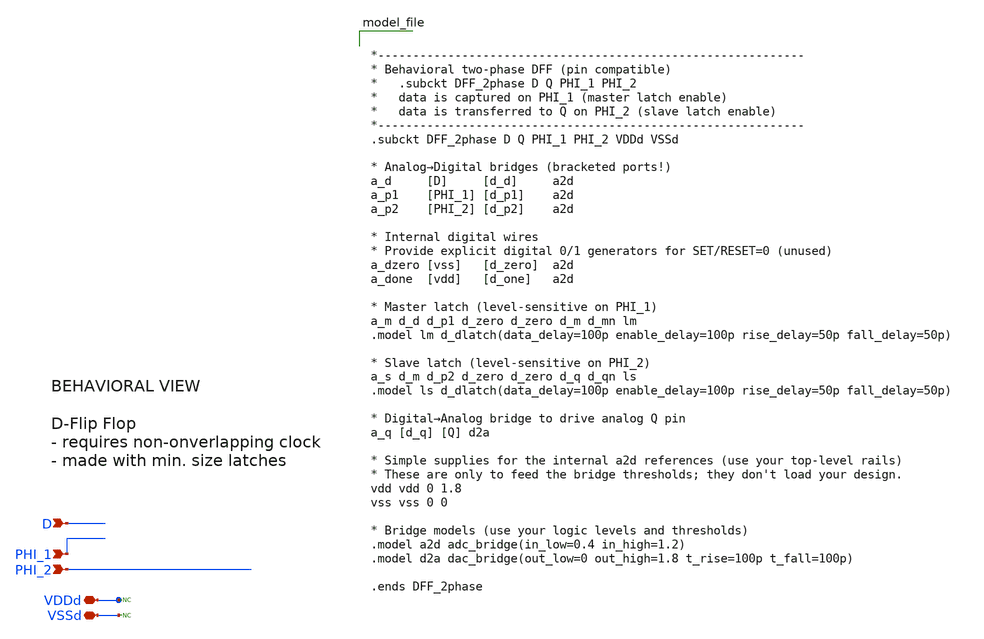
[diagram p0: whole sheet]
** sch_path: DFF_2phase_1/views/DFF_2phase_1_behave.sch
**.subckt DFF_2phase_1_behave D PHI_1 PHI_2 VDDd VSSd
*.ipin D
*.ipin PHI_1
*.ipin PHI_2
*.iopin VDDd
*.iopin VSSd
* noconn VSSd
* noconn VDDd
**** begin user architecture code


*-------------------------------------------------------------
* Behavioral two-phase DFF (pin compatible)
*   .subckt DFF_2phase D Q PHI_1 PHI_2
*   data is captured on PHI_1 (master latch enable)
*   data is transferred to Q on PHI_2 (slave latch enable)
*-------------------------------------------------------------
.subckt DFF_2phase D Q PHI_1 PHI_2 VDDd VSSd

* Analog→Digital bridges (bracketed ports!)
a_d     [D]     [d_d]     a2d
a_p1    [PHI_1] [d_p1]    a2d
a_p2    [PHI_2] [d_p2]    a2d

* Internal digital wires
* Provide explicit digital 0/1 generators for SET/RESET=0 (unused)
a_dzero [vss]   [d_zero]  a2d
a_done  [vdd]   [d_one]   a2d

* Master latch (level-sensitive on PHI_1)
a_m d_d d_p1 d_zero d_zero d_m d_mn lm
.model lm d_dlatch(data_delay=100p enable_delay=100p rise_delay=50p fall_delay=50p)

* Slave latch (level-sensitive on PHI_2)
a_s d_m d_p2 d_zero d_zero d_q d_qn ls
.model ls d_dlatch(data_delay=100p enable_delay=100p rise_delay=50p fall_delay=50p)

* Digital→Analog bridge to drive analog Q pin
a_q [d_q] [Q] d2a

* Simple supplies for the internal a2d references (use your top-level rails)
* These are only to feed the bridge thresholds; they don't load your design.
vdd vdd 0 1.8
vss vss 0 0

* Bridge models (use your logic levels and thresholds)
.model a2d adc_bridge(in_low=0.4 in_high=1.2)
.model d2a dac_bridge(out_low=0 out_high=1.8 t_rise=100p t_fall=100p)

.ends DFF_2phase


**** end user architecture code
**.ends
.end
